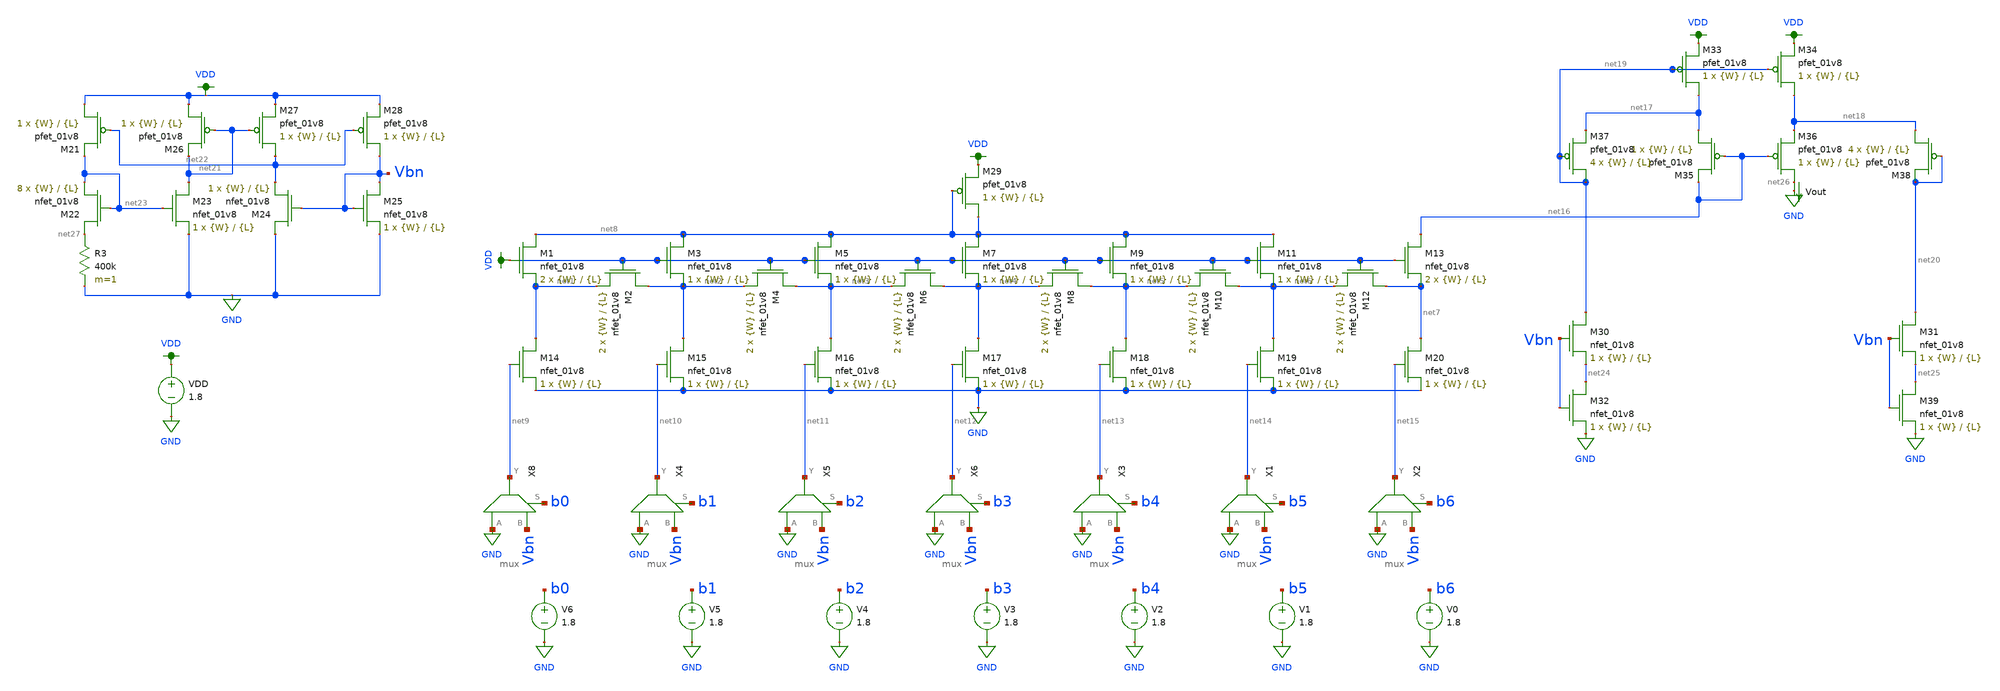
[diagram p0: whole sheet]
** sch_path: schematics/dac_dnl_inl_current_mirror.sch
**.subckt dac_dnl_inl_current_mirror
XM1 net8 VDD net1 GND sky130_fd_pr__nfet_01v8 L={L} W={W} nf=1 ad='int((nf+1)/2) * W/nf * 0.29' as='int((nf+2)/2) * W/nf * 0.29'
+ pd='2*int((nf+1)/2) * (W/nf + 0.29)' ps='2*int((nf+2)/2) * (W/nf + 0.29)' nrd='0.29 / W' nrs='0.29 / W'
+ sa=0 sb=0 sd=0 mult=2 m=2
XM2 net2 VDD net1 GND sky130_fd_pr__nfet_01v8 L={L} W={W} nf=1 ad='int((nf+1)/2) * W/nf * 0.29' as='int((nf+2)/2) * W/nf * 0.29'
+ pd='2*int((nf+1)/2) * (W/nf + 0.29)' ps='2*int((nf+2)/2) * (W/nf + 0.29)' nrd='0.29 / W' nrs='0.29 / W'
+ sa=0 sb=0 sd=0 mult=2 m=2
XM3 net8 VDD net2 GND sky130_fd_pr__nfet_01v8 L={L} W={W} nf=1 ad='int((nf+1)/2) * W/nf * 0.29' as='int((nf+2)/2) * W/nf * 0.29'
+ pd='2*int((nf+1)/2) * (W/nf + 0.29)' ps='2*int((nf+2)/2) * (W/nf + 0.29)' nrd='0.29 / W' nrs='0.29 / W'
+ sa=0 sb=0 sd=0 mult=1 m=1
XM4 net3 VDD net2 GND sky130_fd_pr__nfet_01v8 L={L} W={W} nf=1 ad='int((nf+1)/2) * W/nf * 0.29' as='int((nf+2)/2) * W/nf * 0.29'
+ pd='2*int((nf+1)/2) * (W/nf + 0.29)' ps='2*int((nf+2)/2) * (W/nf + 0.29)' nrd='0.29 / W' nrs='0.29 / W'
+ sa=0 sb=0 sd=0 mult=2 m=2
XM5 net8 VDD net3 GND sky130_fd_pr__nfet_01v8 L={L} W={W} nf=1 ad='int((nf+1)/2) * W/nf * 0.29' as='int((nf+2)/2) * W/nf * 0.29'
+ pd='2*int((nf+1)/2) * (W/nf + 0.29)' ps='2*int((nf+2)/2) * (W/nf + 0.29)' nrd='0.29 / W' nrs='0.29 / W'
+ sa=0 sb=0 sd=0 mult=1 m=1
XM6 net4 VDD net3 GND sky130_fd_pr__nfet_01v8 L={L} W={W} nf=1 ad='int((nf+1)/2) * W/nf * 0.29' as='int((nf+2)/2) * W/nf * 0.29'
+ pd='2*int((nf+1)/2) * (W/nf + 0.29)' ps='2*int((nf+2)/2) * (W/nf + 0.29)' nrd='0.29 / W' nrs='0.29 / W'
+ sa=0 sb=0 sd=0 mult=2 m=2
XM7 net8 VDD net4 GND sky130_fd_pr__nfet_01v8 L={L} W={W} nf=1 ad='int((nf+1)/2) * W/nf * 0.29' as='int((nf+2)/2) * W/nf * 0.29'
+ pd='2*int((nf+1)/2) * (W/nf + 0.29)' ps='2*int((nf+2)/2) * (W/nf + 0.29)' nrd='0.29 / W' nrs='0.29 / W'
+ sa=0 sb=0 sd=0 mult=1 m=1
XM8 net5 VDD net4 GND sky130_fd_pr__nfet_01v8 L={L} W={W} nf=1 ad='int((nf+1)/2) * W/nf * 0.29' as='int((nf+2)/2) * W/nf * 0.29'
+ pd='2*int((nf+1)/2) * (W/nf + 0.29)' ps='2*int((nf+2)/2) * (W/nf + 0.29)' nrd='0.29 / W' nrs='0.29 / W'
+ sa=0 sb=0 sd=0 mult=2 m=2
XM9 net8 VDD net5 GND sky130_fd_pr__nfet_01v8 L={L} W={W} nf=1 ad='int((nf+1)/2) * W/nf * 0.29' as='int((nf+2)/2) * W/nf * 0.29'
+ pd='2*int((nf+1)/2) * (W/nf + 0.29)' ps='2*int((nf+2)/2) * (W/nf + 0.29)' nrd='0.29 / W' nrs='0.29 / W'
+ sa=0 sb=0 sd=0 mult=1 m=1
XM10 net6 VDD net5 GND sky130_fd_pr__nfet_01v8 L={L} W={W} nf=1 ad='int((nf+1)/2) * W/nf * 0.29' as='int((nf+2)/2) * W/nf * 0.29'
+ pd='2*int((nf+1)/2) * (W/nf + 0.29)' ps='2*int((nf+2)/2) * (W/nf + 0.29)' nrd='0.29 / W' nrs='0.29 / W'
+ sa=0 sb=0 sd=0 mult=2 m=2
XM11 net8 VDD net6 GND sky130_fd_pr__nfet_01v8 L={L} W={W} nf=1 ad='int((nf+1)/2) * W/nf * 0.29' as='int((nf+2)/2) * W/nf * 0.29'
+ pd='2*int((nf+1)/2) * (W/nf + 0.29)' ps='2*int((nf+2)/2) * (W/nf + 0.29)' nrd='0.29 / W' nrs='0.29 / W'
+ sa=0 sb=0 sd=0 mult=1 m=1
XM12 net7 VDD net6 GND sky130_fd_pr__nfet_01v8 L={L} W={W} nf=1 ad='int((nf+1)/2) * W/nf * 0.29' as='int((nf+2)/2) * W/nf * 0.29'
+ pd='2*int((nf+1)/2) * (W/nf + 0.29)' ps='2*int((nf+2)/2) * (W/nf + 0.29)' nrd='0.29 / W' nrs='0.29 / W'
+ sa=0 sb=0 sd=0 mult=2 m=2
XM13 net16 VDD net7 GND sky130_fd_pr__nfet_01v8 L={L} W={W} nf=1 ad='int((nf+1)/2) * W/nf * 0.29' as='int((nf+2)/2) * W/nf * 0.29'
+ pd='2*int((nf+1)/2) * (W/nf + 0.29)' ps='2*int((nf+2)/2) * (W/nf + 0.29)' nrd='0.29 / W' nrs='0.29 / W'
+ sa=0 sb=0 sd=0 mult=2 m=2
XM14 net1 net9 GND GND sky130_fd_pr__nfet_01v8 L={L} W={W} nf=1 ad='int((nf+1)/2) * W/nf * 0.29' as='int((nf+2)/2) * W/nf * 0.29'
+ pd='2*int((nf+1)/2) * (W/nf + 0.29)' ps='2*int((nf+2)/2) * (W/nf + 0.29)' nrd='0.29 / W' nrs='0.29 / W'
+ sa=0 sb=0 sd=0 mult=1 m=1
XM15 net2 net10 GND GND sky130_fd_pr__nfet_01v8 L={L} W={W} nf=1 ad='int((nf+1)/2) * W/nf * 0.29' as='int((nf+2)/2) * W/nf * 0.29'
+ pd='2*int((nf+1)/2) * (W/nf + 0.29)' ps='2*int((nf+2)/2) * (W/nf + 0.29)' nrd='0.29 / W' nrs='0.29 / W'
+ sa=0 sb=0 sd=0 mult=1 m=1
XM16 net3 net11 GND GND sky130_fd_pr__nfet_01v8 L={L} W={W} nf=1 ad='int((nf+1)/2) * W/nf * 0.29' as='int((nf+2)/2) * W/nf * 0.29'
+ pd='2*int((nf+1)/2) * (W/nf + 0.29)' ps='2*int((nf+2)/2) * (W/nf + 0.29)' nrd='0.29 / W' nrs='0.29 / W'
+ sa=0 sb=0 sd=0 mult=1 m=1
XM17 net4 net12 GND GND sky130_fd_pr__nfet_01v8 L={L} W={W} nf=1 ad='int((nf+1)/2) * W/nf * 0.29' as='int((nf+2)/2) * W/nf * 0.29'
+ pd='2*int((nf+1)/2) * (W/nf + 0.29)' ps='2*int((nf+2)/2) * (W/nf + 0.29)' nrd='0.29 / W' nrs='0.29 / W'
+ sa=0 sb=0 sd=0 mult=1 m=1
XM18 net5 net13 GND GND sky130_fd_pr__nfet_01v8 L={L} W={W} nf=1 ad='int((nf+1)/2) * W/nf * 0.29' as='int((nf+2)/2) * W/nf * 0.29'
+ pd='2*int((nf+1)/2) * (W/nf + 0.29)' ps='2*int((nf+2)/2) * (W/nf + 0.29)' nrd='0.29 / W' nrs='0.29 / W'
+ sa=0 sb=0 sd=0 mult=1 m=1
XM19 net6 net14 GND GND sky130_fd_pr__nfet_01v8 L={L} W={W} nf=1 ad='int((nf+1)/2) * W/nf * 0.29' as='int((nf+2)/2) * W/nf * 0.29'
+ pd='2*int((nf+1)/2) * (W/nf + 0.29)' ps='2*int((nf+2)/2) * (W/nf + 0.29)' nrd='0.29 / W' nrs='0.29 / W'
+ sa=0 sb=0 sd=0 mult=1 m=1
XM20 net7 net15 GND GND sky130_fd_pr__nfet_01v8 L={L} W={W} nf=1 ad='int((nf+1)/2) * W/nf * 0.29' as='int((nf+2)/2) * W/nf * 0.29'
+ pd='2*int((nf+1)/2) * (W/nf + 0.29)' ps='2*int((nf+2)/2) * (W/nf + 0.29)' nrd='0.29 / W' nrs='0.29 / W'
+ sa=0 sb=0 sd=0 mult=1 m=1
V0 b6 GND 1.8
V1 b5 GND 1.8
V2 b4 GND 1.8
V3 b3 GND 1.8
V4 b2 GND 1.8
V5 b1 GND 1.8
V6 b0 GND 1.8
Vout net26 GND 0
.save i(vout)
VDD VDD GND 1.8
XM33 net17 net19 VDD VDD sky130_fd_pr__pfet_01v8 L={L} W={W} nf=1 ad='int((nf+1)/2) * W/nf * 0.29' as='int((nf+2)/2) * W/nf * 0.29'
+ pd='2*int((nf+1)/2) * (W/nf + 0.29)' ps='2*int((nf+2)/2) * (W/nf + 0.29)' nrd='0.29 / W' nrs='0.29 / W'
+ sa=0 sb=0 sd=0 mult=1 m=1
XM34 net18 net19 VDD VDD sky130_fd_pr__pfet_01v8 L={L} W={W} nf=1 ad='int((nf+1)/2) * W/nf * 0.29' as='int((nf+2)/2) * W/nf * 0.29'
+ pd='2*int((nf+1)/2) * (W/nf + 0.29)' ps='2*int((nf+2)/2) * (W/nf + 0.29)' nrd='0.29 / W' nrs='0.29 / W'
+ sa=0 sb=0 sd=0 mult=1 m=1
XM35 net17 net16 net16 VDD sky130_fd_pr__pfet_01v8 L={L} W={W} nf=1 ad='int((nf+1)/2) * W/nf * 0.29'
+ as='int((nf+2)/2) * W/nf * 0.29' pd='2*int((nf+1)/2) * (W/nf + 0.29)' ps='2*int((nf+2)/2) * (W/nf + 0.29)'
+ nrd='0.29 / W' nrs='0.29 / W' sa=0 sb=0 sd=0 mult=1 m=1
XM36 net26 net16 net18 VDD sky130_fd_pr__pfet_01v8 L={L} W={W} nf=1 ad='int((nf+1)/2) * W/nf * 0.29'
+ as='int((nf+2)/2) * W/nf * 0.29' pd='2*int((nf+1)/2) * (W/nf + 0.29)' ps='2*int((nf+2)/2) * (W/nf + 0.29)'
+ nrd='0.29 / W' nrs='0.29 / W' sa=0 sb=0 sd=0 mult=1 m=1
XM37 net19 net19 net17 VDD sky130_fd_pr__pfet_01v8 L={L} W={W} nf=1 ad='int((nf+1)/2) * W/nf * 0.29'
+ as='int((nf+2)/2) * W/nf * 0.29' pd='2*int((nf+1)/2) * (W/nf + 0.29)' ps='2*int((nf+2)/2) * (W/nf + 0.29)'
+ nrd='0.29 / W' nrs='0.29 / W' sa=0 sb=0 sd=0 mult=4 m=4
XM38 net18 net20 net20 VDD sky130_fd_pr__pfet_01v8 L={L} W={W} nf=1 ad='int((nf+1)/2) * W/nf * 0.29'
+ as='int((nf+2)/2) * W/nf * 0.29' pd='2*int((nf+1)/2) * (W/nf + 0.29)' ps='2*int((nf+2)/2) * (W/nf + 0.29)'
+ nrd='0.29 / W' nrs='0.29 / W' sa=0 sb=0 sd=0 mult=4 m=4
XM21 VDD net22 net23 VDD sky130_fd_pr__pfet_01v8 L={L} W={W} nf=1 ad='int((nf+1)/2) * W/nf * 0.29' as='int((nf+2)/2) * W/nf * 0.29'
+ pd='2*int((nf+1)/2) * (W/nf + 0.29)' ps='2*int((nf+2)/2) * (W/nf + 0.29)' nrd='0.29 / W' nrs='0.29 / W'
+ sa=0 sb=0 sd=0 mult=1 m=1
XM22 net27 net23 net23 GND sky130_fd_pr__nfet_01v8 L={L} W={W} nf=1 ad='int((nf+1)/2) * W/nf * 0.29'
+ as='int((nf+2)/2) * W/nf * 0.29' pd='2*int((nf+1)/2) * (W/nf + 0.29)' ps='2*int((nf+2)/2) * (W/nf + 0.29)'
+ nrd='0.29 / W' nrs='0.29 / W' sa=0 sb=0 sd=0 mult=8 m=8
R3 net27 GND 400k m=1
XM23 net21 net23 GND GND sky130_fd_pr__nfet_01v8 L={L} W={W} nf=1 ad='int((nf+1)/2) * W/nf * 0.29' as='int((nf+2)/2) * W/nf * 0.29'
+ pd='2*int((nf+1)/2) * (W/nf + 0.29)' ps='2*int((nf+2)/2) * (W/nf + 0.29)' nrd='0.29 / W' nrs='0.29 / W'
+ sa=0 sb=0 sd=0 mult=1 m=1
XM24 GND Vbn net22 GND sky130_fd_pr__nfet_01v8 L={L} W={W} nf=1 ad='int((nf+1)/2) * W/nf * 0.29' as='int((nf+2)/2) * W/nf * 0.29'
+ pd='2*int((nf+1)/2) * (W/nf + 0.29)' ps='2*int((nf+2)/2) * (W/nf + 0.29)' nrd='0.29 / W' nrs='0.29 / W'
+ sa=0 sb=0 sd=0 mult=1 m=1
XM25 Vbn Vbn GND GND sky130_fd_pr__nfet_01v8 L={L} W={W} nf=1 ad='int((nf+1)/2) * W/nf * 0.29' as='int((nf+2)/2) * W/nf * 0.29'
+ pd='2*int((nf+1)/2) * (W/nf + 0.29)' ps='2*int((nf+2)/2) * (W/nf + 0.29)' nrd='0.29 / W' nrs='0.29 / W'
+ sa=0 sb=0 sd=0 mult=1 m=1
XM26 VDD net21 net21 VDD sky130_fd_pr__pfet_01v8 L={L} W={W} nf=1 ad='int((nf+1)/2) * W/nf * 0.29' as='int((nf+2)/2) * W/nf * 0.29'
+ pd='2*int((nf+1)/2) * (W/nf + 0.29)' ps='2*int((nf+2)/2) * (W/nf + 0.29)' nrd='0.29 / W' nrs='0.29 / W'
+ sa=0 sb=0 sd=0 mult=1 m=1
XM27 net22 net21 VDD VDD sky130_fd_pr__pfet_01v8 L={L} W={W} nf=1 ad='int((nf+1)/2) * W/nf * 0.29' as='int((nf+2)/2) * W/nf * 0.29'
+ pd='2*int((nf+1)/2) * (W/nf + 0.29)' ps='2*int((nf+2)/2) * (W/nf + 0.29)' nrd='0.29 / W' nrs='0.29 / W'
+ sa=0 sb=0 sd=0 mult=1 m=1
XM28 Vbn net22 VDD VDD sky130_fd_pr__pfet_01v8 L={L} W={W} nf=1 ad='int((nf+1)/2) * W/nf * 0.29' as='int((nf+2)/2) * W/nf * 0.29'
+ pd='2*int((nf+1)/2) * (W/nf + 0.29)' ps='2*int((nf+2)/2) * (W/nf + 0.29)' nrd='0.29 / W' nrs='0.29 / W'
+ sa=0 sb=0 sd=0 mult=1 m=1
XM29 net8 net8 VDD VDD sky130_fd_pr__pfet_01v8 L={L} W={W} nf=1 ad='int((nf+1)/2) * W/nf * 0.29' as='int((nf+2)/2) * W/nf * 0.29'
+ pd='2*int((nf+1)/2) * (W/nf + 0.29)' ps='2*int((nf+2)/2) * (W/nf + 0.29)' nrd='0.29 / W' nrs='0.29 / W'
+ sa=0 sb=0 sd=0 mult=1 m=1
XM30 net19 Vbn net24 GND sky130_fd_pr__nfet_01v8 L={L} W={W} nf=1 ad='int((nf+1)/2) * W/nf * 0.29' as='int((nf+2)/2) * W/nf * 0.29'
+ pd='2*int((nf+1)/2) * (W/nf + 0.29)' ps='2*int((nf+2)/2) * (W/nf + 0.29)' nrd='0.29 / W' nrs='0.29 / W'
+ sa=0 sb=0 sd=0 mult=1 m=1
XM31 net20 Vbn net25 GND sky130_fd_pr__nfet_01v8 L={L} W={W} nf=1 ad='int((nf+1)/2) * W/nf * 0.29' as='int((nf+2)/2) * W/nf * 0.29'
+ pd='2*int((nf+1)/2) * (W/nf + 0.29)' ps='2*int((nf+2)/2) * (W/nf + 0.29)' nrd='0.29 / W' nrs='0.29 / W'
+ sa=0 sb=0 sd=0 mult=1 m=1
XM32 net24 Vbn GND GND sky130_fd_pr__nfet_01v8 L={L} W={W} nf=1 ad='int((nf+1)/2) * W/nf * 0.29' as='int((nf+2)/2) * W/nf * 0.29'
+ pd='2*int((nf+1)/2) * (W/nf + 0.29)' ps='2*int((nf+2)/2) * (W/nf + 0.29)' nrd='0.29 / W' nrs='0.29 / W'
+ sa=0 sb=0 sd=0 mult=1 m=1
XM39 net25 Vbn GND GND sky130_fd_pr__nfet_01v8 L={L} W={W} nf=1 ad='int((nf+1)/2) * W/nf * 0.29' as='int((nf+2)/2) * W/nf * 0.29'
+ pd='2*int((nf+1)/2) * (W/nf + 0.29)' ps='2*int((nf+2)/2) * (W/nf + 0.29)' nrd='0.29 / W' nrs='0.29 / W'
+ sa=0 sb=0 sd=0 mult=1 m=1
X8 GND Vbn net9 b0 mux
X4 GND Vbn net10 b1 mux
X5 GND Vbn net11 b2 mux
X6 GND Vbn net12 b3 mux
X3 GND Vbn net13 b4 mux
X1 GND Vbn net14 b5 mux
X2 GND Vbn net15 b6 mux
**** begin user architecture code

.param W=1
.param L=4
.control
set wr_vecnames
set wr_singlescale
let code = 0
  while code < 128
    if code eq 0
      let b0 = 0
    else
      let b0 = 1.8
    end
    if floor(code / 2) eq 0
      let b1 = 0
    else
      let b1 = 1.8
    end
    if floor(code / 4) eq 0
      let b2 = 0
    else
      let b2 = 1.8
    end
    if floor(code / 8) eq 0
      let b3 = 0
    else
      let b3 = 1.8
    end
    if floor(code / 16) eq 0
      let b4 = 0
    else
      let b4 = 1.8
    end
    if floor(code / 32) eq 0
      let b5 = 0
    else
      let b5 = 1.8
    end
    if floor(code / 64) eq 0
      let b6 = 0
    else
      let b6 = 1.8
    end
    alter v0 $&b0
    alter v1 $&b1
    alter v2 $&b2
    alter v3 $&b3
    alter v4 $&b4
    alter v5 $&b5
    alter v6 $&b6
    save all
    op
    wrdata ~/current-output-dac-vlsi/simulations/dac_sim.txt i(Vout) v(b5) v(b6) v(b4) v(b3) v(b2)
+ v(b1) v(b0)
    if code eq 0
      set appendwrite
      set wr_vecnames = FALSE
    end
    let code = code + 1
  end
.endc


.option wnflag=1
.param MC_SWITCH=0.0
.lib ~/skywater/skywater-pdk/libraries/sky130_fd_pr_ngspice/latest/models/sky130.lib.spice tt

**** end user architecture code
**.ends

* expanding   symbol:  /home/madvlsi/Documents/current-output-dac-vlsi/schematics/mux.sym # of
*+ pins=4
** sym_path: /home/madvlsi/Documents/current-output-dac-vlsi/schematics/mux.sym
** sch_path: /home/madvlsi/Documents/current-output-dac-vlsi/schematics/mux.sch
.subckt mux A B Y S
*.ipin S
*.ipin A
*.opin Y
*.ipin B
XM1 net1 S GND GND sky130_fd_pr__nfet_01v8 L=0.15 W=1 nf=1 ad='int((nf+1)/2) * W/nf * 0.29' as='int((nf+2)/2) * W/nf * 0.29'
+ pd='2*int((nf+1)/2) * (W/nf + 0.29)' ps='2*int((nf+2)/2) * (W/nf + 0.29)' nrd='0.29 / W' nrs='0.29 / W'
+ sa=0 sb=0 sd=0 mult=1 m=1
XM2 net1 S VDD VDD sky130_fd_pr__pfet_01v8 L=0.15 W=1 nf=1 ad='int((nf+1)/2) * W/nf * 0.29' as='int((nf+2)/2) * W/nf * 0.29'
+ pd='2*int((nf+1)/2) * (W/nf + 0.29)' ps='2*int((nf+2)/2) * (W/nf + 0.29)' nrd='0.29 / W' nrs='0.29 / W'
+ sa=0 sb=0 sd=0 mult=1 m=1
XM3 Y S B GND sky130_fd_pr__nfet_01v8 L=0.15 W=1 nf=1 ad='int((nf+1)/2) * W/nf * 0.29' as='int((nf+2)/2) * W/nf * 0.29'
+ pd='2*int((nf+1)/2) * (W/nf + 0.29)' ps='2*int((nf+2)/2) * (W/nf + 0.29)' nrd='0.29 / W' nrs='0.29 / W'
+ sa=0 sb=0 sd=0 mult=1 m=1
XM4 A net1 Y GND sky130_fd_pr__nfet_01v8 L=0.15 W=1 nf=1 ad='int((nf+1)/2) * W/nf * 0.29' as='int((nf+2)/2) * W/nf * 0.29'
+ pd='2*int((nf+1)/2) * (W/nf + 0.29)' ps='2*int((nf+2)/2) * (W/nf + 0.29)' nrd='0.29 / W' nrs='0.29 / W'
+ sa=0 sb=0 sd=0 mult=1 m=1
.ends

.GLOBAL GND
.GLOBAL VDD
.end
